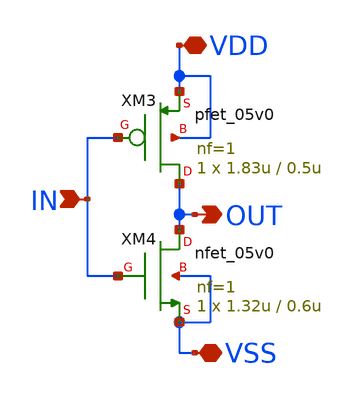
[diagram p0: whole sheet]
** sch_path: FINAL/XSCHEM/WEIGTH/INV_1.sch
**.subckt INV_1 IN VDD OUT VSS
*.ipin IN
*.iopin VDD
*.opin OUT
*.iopin VSS
XM3 OUT IN VDD VDD pfet_05v0 L=0.5u W=1.83u nf=1 ad='int((nf+1)/2) * W/nf * 0.18u' as='int((nf+2)/2) * W/nf * 0.18u'
+ pd='2*int((nf+1)/2) * (W/nf + 0.18u)' ps='2*int((nf+2)/2) * (W/nf + 0.18u)' nrd='0.18u / W' nrs='0.18u / W'
+ sa=0 sb=0 sd=0 m=1
XM4 OUT IN VSS VSS nfet_05v0 L=0.6u W=1.32u nf=1 ad='int((nf+1)/2) * W/nf * 0.18u' as='int((nf+2)/2) * W/nf * 0.18u'
+ pd='2*int((nf+1)/2) * (W/nf + 0.18u)' ps='2*int((nf+2)/2) * (W/nf + 0.18u)' nrd='0.18u / W' nrs='0.18u / W'
+ sa=0 sb=0 sd=0 m=1
**.ends
.end
